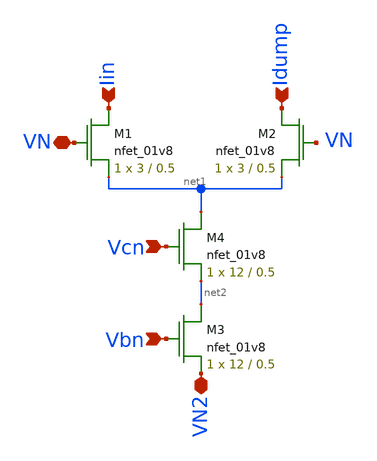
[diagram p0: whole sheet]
** sch_path: lvs/dummy_current_steering_cell.sch
**.subckt dummy_current_steering_cell VN2 Vcn Iin Idump Vbn VN
*.iopin VN2
*.ipin Vcn
*.ipin Iin
*.ipin Idump
*.ipin Vbn
*.iopin VN
XM1 Iin VN net1 GND sky130_fd_pr__nfet_01v8 L=0.5 W=3 nf=1 ad='int((nf+1)/2) * W/nf * 0.29' as='int((nf+2)/2) * W/nf * 0.29'
+ pd='2*int((nf+1)/2) * (W/nf + 0.29)' ps='2*int((nf+2)/2) * (W/nf + 0.29)' nrd='0.29 / W' nrs='0.29 / W'
+ sa=0 sb=0 sd=0 mult=1 m=1
XM2 Idump VN net1 GND sky130_fd_pr__nfet_01v8 L=0.5 W=3 nf=1 ad='int((nf+1)/2) * W/nf * 0.29' as='int((nf+2)/2) * W/nf * 0.29'
+ pd='2*int((nf+1)/2) * (W/nf + 0.29)' ps='2*int((nf+2)/2) * (W/nf + 0.29)' nrd='0.29 / W' nrs='0.29 / W'
+ sa=0 sb=0 sd=0 mult=1 m=1
XM3 net2 Vbn VN2 GND sky130_fd_pr__nfet_01v8 L=0.5 W=12 nf=1 ad='int((nf+1)/2) * W/nf * 0.29' as='int((nf+2)/2) * W/nf * 0.29'
+ pd='2*int((nf+1)/2) * (W/nf + 0.29)' ps='2*int((nf+2)/2) * (W/nf + 0.29)' nrd='0.29 / W' nrs='0.29 / W'
+ sa=0 sb=0 sd=0 mult=1 m=1
XM4 net1 Vcn net2 GND sky130_fd_pr__nfet_01v8 L=0.5 W=12 nf=1 ad='int((nf+1)/2) * W/nf * 0.29' as='int((nf+2)/2) * W/nf * 0.29'
+ pd='2*int((nf+1)/2) * (W/nf + 0.29)' ps='2*int((nf+2)/2) * (W/nf + 0.29)' nrd='0.29 / W' nrs='0.29 / W'
+ sa=0 sb=0 sd=0 mult=1 m=1
**.ends
.end
